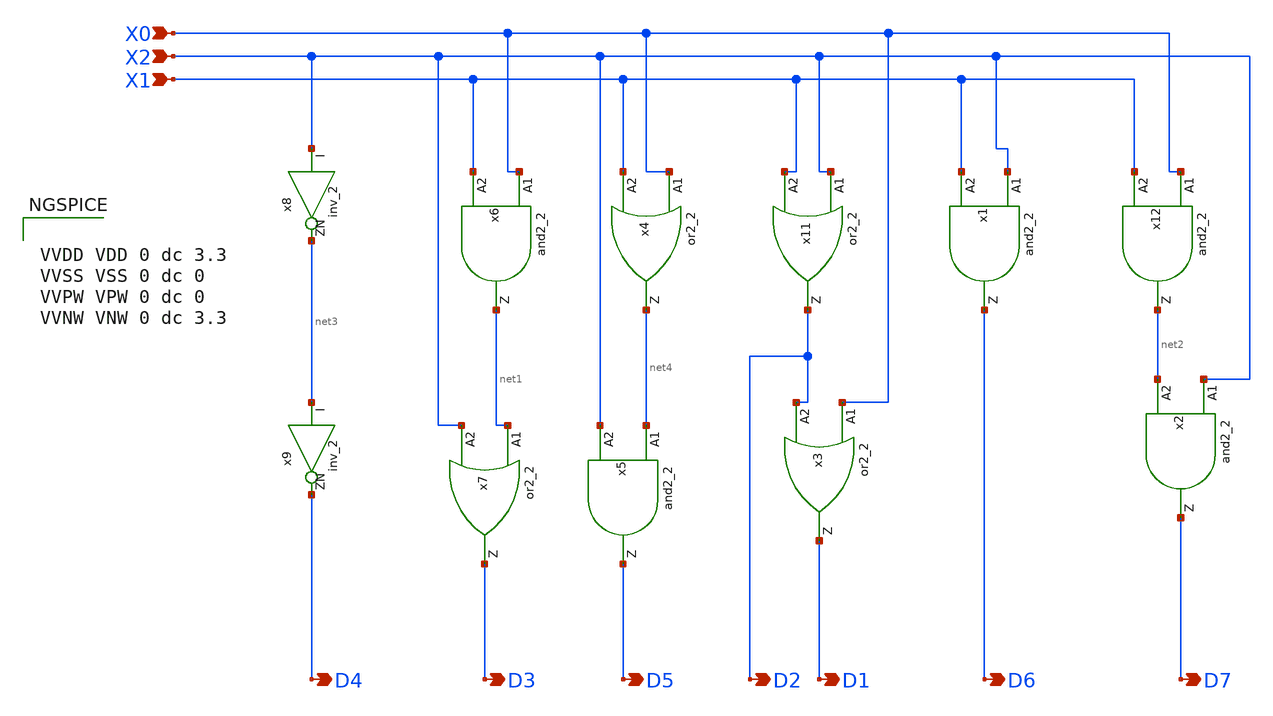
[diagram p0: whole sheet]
** sch_path: xschem/thermometter_decoder.sch
**.subckt thermometter_decoder X0 X1 X2 D1 D2 D3 D4 D5 D6 D7
*.ipin X0
*.ipin X1
*.ipin X2
*.opin D1
*.opin D2
*.opin D3
*.opin D4
*.opin D5
*.opin D6
*.opin D7
x3 X0 D2 D1 VDD VNW VPW VSS gf180mcu_fd_sc_mcu7t5v0__or2_2
x4 X0 X1 net4 VDD VNW VPW VSS gf180mcu_fd_sc_mcu7t5v0__or2_2
x5 net4 X2 D5 VDD VNW VPW VSS gf180mcu_fd_sc_mcu7t5v0__and2_2
x6 X0 X1 net1 VDD VNW VPW VSS gf180mcu_fd_sc_mcu7t5v0__and2_2
x7 net1 X2 D3 VDD VNW VPW VSS gf180mcu_fd_sc_mcu7t5v0__or2_2
x8 X2 net3 VDD VNW VPW VSS gf180mcu_fd_sc_mcu7t5v0__inv_2
x9 net3 D4 VDD VNW VPW VSS gf180mcu_fd_sc_mcu7t5v0__inv_2
x12 X0 X1 net2 VDD VNW VPW VSS gf180mcu_fd_sc_mcu7t5v0__and2_2
x1 X2 X1 D6 VDD VNW VPW VSS gf180mcu_fd_sc_mcu7t5v0__and2_2
x2 X2 net2 D7 VDD VNW VPW VSS gf180mcu_fd_sc_mcu7t5v0__and2_2
x11 X2 X1 D2 VDD VNW VPW VSS gf180mcu_fd_sc_mcu7t5v0__or2_2
**** begin user architecture code


VVDD VDD 0 dc 3.3
VVSS VSS 0 dc 0
VVPW VPW 0 dc 0
VVNW VNW 0 dc 3.3


**** end user architecture code
**.ends
.end
